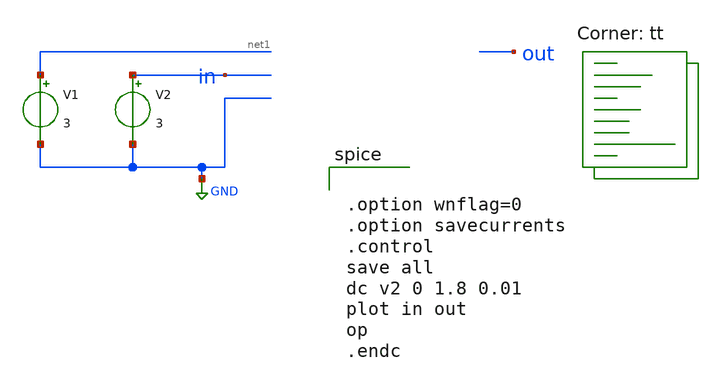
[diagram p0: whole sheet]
** sch_path: Inverterterbaru/xschem/last.sch
**.subckt last
V1 net1 GND 3
V2 in GND 3
**** begin user architecture code
.lib $::SKYWATER_MODELS/sky130.lib.spice tt


.option wnflag=0
.option savecurrents
.control
save all
dc v2 0 1.8 0.01
plot in out
op
.endc


**** end user architecture code
**.ends
.GLOBAL GND
.end
